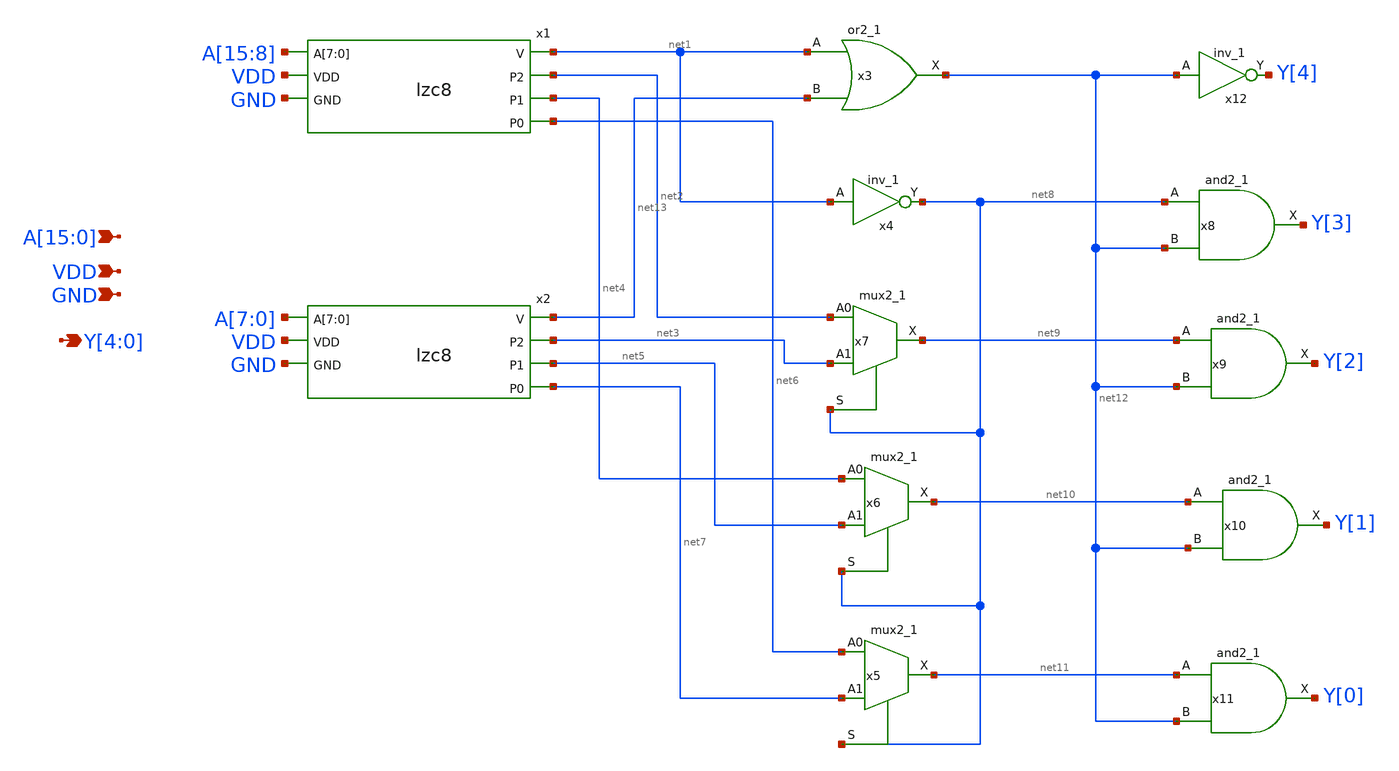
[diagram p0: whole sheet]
** sch_path: frontend/xschem/lzc16.sch
**.subckt lzc16
*+ A[15],A[14],A[13],A[12],A[11],A[10],A[9],A[8],A[7],A[6],A[5],A[4],A[3],A[2],A[1],A[0] VDD GND Y[4],Y[3],Y[2],Y[1],Y[0]
*.ipin A[15],A[14],A[13],A[12],A[11],A[10],A[9],A[8],A[7],A[6],A[5],A[4],A[3],A[2],A[1],A[0]
*.ipin VDD
*.ipin GND
*.opin Y[4],Y[3],Y[2],Y[1],Y[0]
x1 A[15] A[14] A[13] A[12] A[11] A[10] A[9] A[8] net1 net2 VDD GND net4 net6 lzc8
x2 A[7] A[6] A[5] A[4] A[3] A[2] A[1] A[0] net13 net3 VDD GND net5 net7 lzc8
x3 net1 net13 GND GND VDD VDD net12 sky130_fd_sc_hd__or2_1
x4 net1 GND GND VDD VDD net8 sky130_fd_sc_hd__inv_1
x5 net6 net7 net8 GND GND VDD VDD net11 sky130_fd_sc_hd__mux2_1
x6 net4 net5 net8 GND GND VDD VDD net10 sky130_fd_sc_hd__mux2_1
x7 net2 net3 net8 GND GND VDD VDD net9 sky130_fd_sc_hd__mux2_1
x8 net8 net12 GND GND VDD VDD Y[3] sky130_fd_sc_hd__and2_1
x9 net9 net12 GND GND VDD VDD Y[2] sky130_fd_sc_hd__and2_1
x10 net10 net12 GND GND VDD VDD Y[1] sky130_fd_sc_hd__and2_1
x11 net11 net12 GND GND VDD VDD Y[0] sky130_fd_sc_hd__and2_1
x12 net12 GND GND VDD VDD Y[4] sky130_fd_sc_hd__inv_1
**.ends

* expanding   symbol:  lzc8.sym # of pins=7
** sym_path: frontend/xschem/lzc8.sym
** sch_path: frontend/xschem/lzc8.sch
.subckt lzc8 A[7] A[6] A[5] A[4] A[3] A[2] A[1] A[0] V P2 VDD GND P1 P0
*.opin V
*.opin P2
*.opin P1
*.opin P0
*.ipin VDD
*.ipin GND
*.ipin A[7],A[6],A[5],A[4],A[3],A[2],A[1],A[0]
x1 A[7] A[6] A[5] A[4] net1 VDD net2 GND net5 lzc4
x2 A[3] A[2] A[1] A[0] net3 VDD net4 GND net6 lzc4
x3 net1 net3 GND GND VDD VDD V sky130_fd_sc_hd__or2_1
x4 net1 GND GND VDD VDD P2 sky130_fd_sc_hd__inv_1
x5 net2 net4 P2 GND GND VDD VDD P1 sky130_fd_sc_hd__mux2_1
x6 net5 net6 P2 GND GND VDD VDD P0 sky130_fd_sc_hd__mux2_1
.ends


* expanding   symbol:  lzc4.sym # of pins=6
** sym_path: frontend/xschem/lzc4.sym
** sch_path: frontend/xschem/lzc4.sch
.subckt lzc4 A[3] A[2] A[1] A[0] V VDD P1 GND P0
*.ipin A[3],A[2],A[1],A[0]
*.opin V
*.opin P1
*.opin P0
*.ipin VDD
*.ipin GND
x1 A[3] net1 A[2] VDD net3 GND lzc2
x2 A[1] net2 A[0] VDD net4 GND lzc2
x3 net1 net2 GND GND VDD VDD V sky130_fd_sc_hd__or2_1
x4 net1 GND GND VDD VDD P1 sky130_fd_sc_hd__inv_1
x5 net3 net4 P1 GND GND VDD VDD P0 sky130_fd_sc_hd__mux2_1
.ends


* expanding   symbol:  lzc2.sym # of pins=6
** sym_path: frontend/xschem/lzc2.sym
** sch_path: frontend/xschem/lzc2.sch
.subckt lzc2 HI V LO VDD P GND
*.ipin HI
*.ipin LO
*.opin V
*.opin P
*.ipin VDD
*.ipin GND
x1 HI LO GND GND VDD VDD V sky130_fd_sc_hd__or2_1
x2 HI GND GND VDD VDD P sky130_fd_sc_hd__inv_1
.ends

.end
